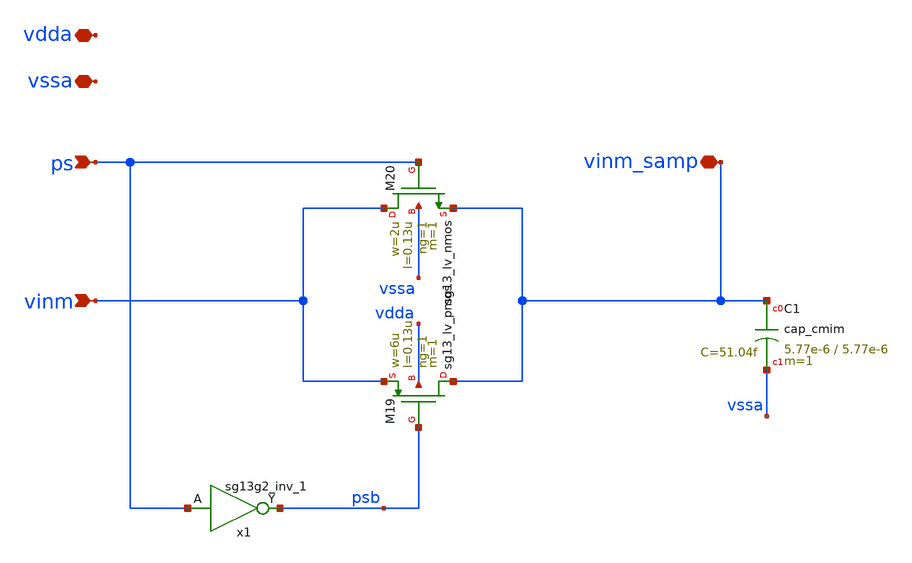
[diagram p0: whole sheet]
** sch_path: 5_Design/4_Layout/Team 5/xschem/comp_5_split3.sch
**.subckt comp_5_split3 vdda vssa ps vinm vinm_samp
*.iopin vdda
*.iopin vssa
*.ipin ps
*.ipin vinm
*.iopin vinm_samp
XM19 vinm_samp psb vinm vdda sg13_lv_pmos w=6u l=0.13u ng=1 m=1 mm_ok=1
XM20 vinm ps vinm_samp vssa sg13_lv_nmos w=2u l=0.13u ng=1 m=1 mm_ok=1
x1 psb ps VDD VSS sg13g2_inv_1
XC1 vinm_samp vssa cap_cmim w=5.77e-6 l=5.77e-6 m=1 mm_ok=1
**.ends

* expanding   symbol:  sg13g2_stdcells/sg13g2_inv_1.sym # of pins=2
** sym_path: sg13g2_stdcells/sg13g2_inv_1.sym
** sch_path: sg13g2_stdcells/sg13g2_inv_1.sch
.subckt sg13g2_inv_1 Y A VDD VSS
*.opin Y
*.ipin A
*.iopin VDD
*.iopin VSS
XM1 Y A VSS VSS sg13_lv_nmos w=740.00n l=130.00n ng=1 m=1 mm_ok=1
XM2 Y A VDD VDD sg13_lv_pmos w=1.12u l=130.00n ng=1 m=1 mm_ok=1
.ends

.end
